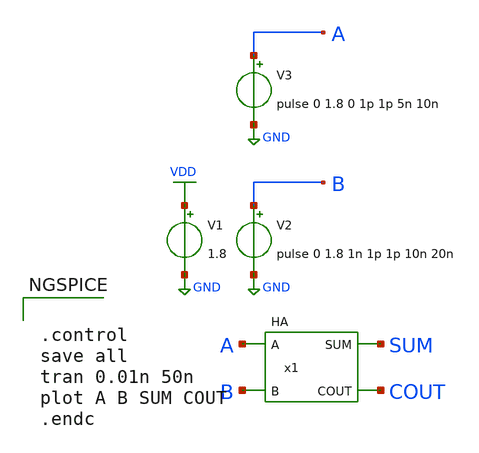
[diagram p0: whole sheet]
** sch_path: current/xschem/test_HA.sch
**.subckt test_HA
V2 B GND pulse 0 1.8 1n 1p 1p 10n 20n
V1 VDD GND 1.8
V3 A GND pulse 0 1.8 0 1p 1p 5n 10n
x1 SUM COUT A B VDD GND HA
**** begin user architecture code

.lib $::SKYWATER_MODELS/sky130.lib.spice tt


**** end user architecture code
**.ends
.GLOBAL VDD
.GLOBAL GND
**** begin user architecture code


.control
save all
tran 0.01n 50n
plot A B SUM COUT
.endc


**** end user architecture code
.end
